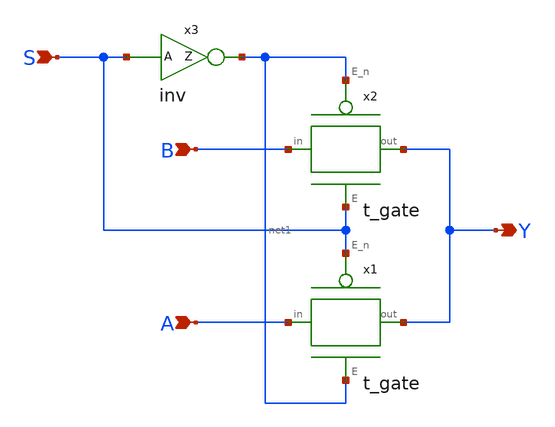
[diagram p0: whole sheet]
** sch_path: xschem/mux21.sch
**.subckt mux21 S A B Y
*.ipin S
*.ipin A
*.ipin B
*.opin Y
x1 S A Y net1 t_gate
x2 net1 B Y S t_gate
x3 net1 S inv
**.ends

* expanding   symbol:  t_gate.sym # of pins=4
** sym_path: xschem/t_gate.sym
** sch_path: xschem/t_gate.sch
.subckt t_gate E_n in out E
*.ipin in
*.opin out
*.ipin E
*.ipin E_n
XM1 in E out GND sky130_fd_pr__nfet_01v8 L=0.15 W=0.42 nf=1 ad='int((nf+1)/2) * W/nf * 0.29' as='int((nf+2)/2) * W/nf * 0.29'
+ pd='2*int((nf+1)/2) * (W/nf + 0.29)' ps='2*int((nf+2)/2) * (W/nf + 0.29)' nrd='0.29 / W' nrs='0.29 / W'
+ sa=0 sb=0 sd=0 mult=1 m=1
XM2 in E_n out VDD sky130_fd_pr__pfet_01v8 L=0.15 W=0.84 nf=1 ad='int((nf+1)/2) * W/nf * 0.29' as='int((nf+2)/2) * W/nf * 0.29'
+ pd='2*int((nf+1)/2) * (W/nf + 0.29)' ps='2*int((nf+2)/2) * (W/nf + 0.29)' nrd='0.29 / W' nrs='0.29 / W'
+ sa=0 sb=0 sd=0 mult=1 m=1
.ends


* expanding   symbol:  inv.sym # of pins=2
** sym_path: xschem/inv.sym
** sch_path: xschem/inv.sch
.subckt inv Z A
*.ipin a
*.opin z
XM1 z a GND GND sky130_fd_pr__nfet_01v8 L=0.15 W=0.42 nf=1 ad='int((nf+1)/2) * W/nf * 0.29' as='int((nf+2)/2) * W/nf * 0.29'
+ pd='2*int((nf+1)/2) * (W/nf + 0.29)' ps='2*int((nf+2)/2) * (W/nf + 0.29)' nrd='0.29 / W' nrs='0.29 / W'
+ sa=0 sb=0 sd=0 mult=1 m=1
XM2 z a VDD VDD sky130_fd_pr__pfet_01v8 L=0.15 W=0.84 nf=1 ad='int((nf+1)/2) * W/nf * 0.29' as='int((nf+2)/2) * W/nf * 0.29'
+ pd='2*int((nf+1)/2) * (W/nf + 0.29)' ps='2*int((nf+2)/2) * (W/nf + 0.29)' nrd='0.29 / W' nrs='0.29 / W'
+ sa=0 sb=0 sd=0 mult=1 m=1
.ends

.GLOBAL GND
.GLOBAL VDD
.end
